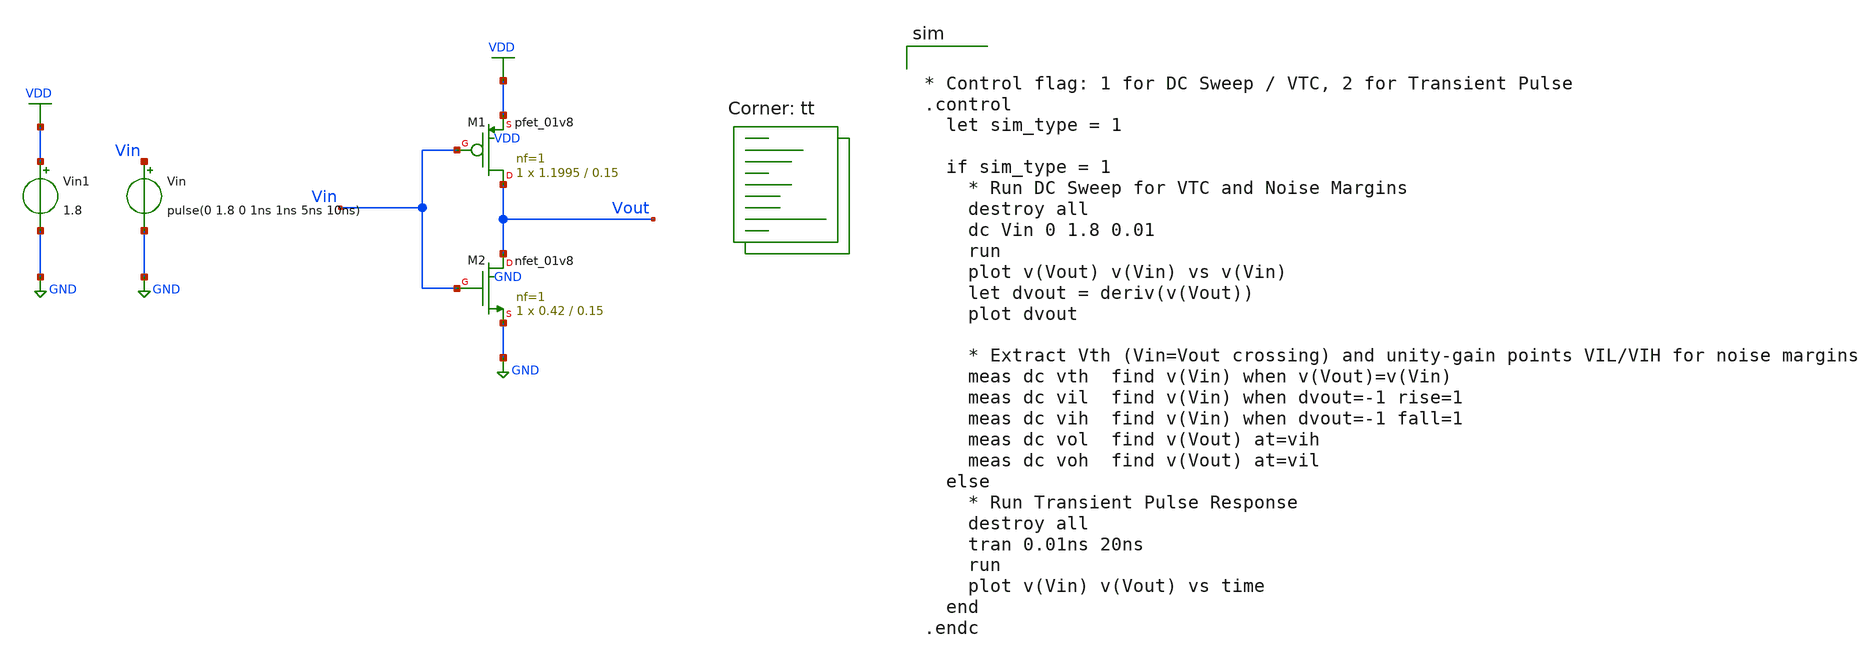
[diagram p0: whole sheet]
** sch_path: assignments/assignment2/assign1a.sch
**.subckt assign1a
Vin Vin GND pulse(0 1.8 0 1ns 1ns 5ns 10ns)
XM1 Vout Vin VDD VDD sky130_fd_pr__pfet_01v8 L=0.15 W=1.1995 nf=1 ad='int((nf+1)/2) * W/nf * 0.29' as='int((nf+2)/2) * W/nf * 0.29'
+ pd='2*int((nf+1)/2) * (W/nf + 0.29)' ps='2*int((nf+2)/2) * (W/nf + 0.29)' nrd='0.29 / W' nrs='0.29 / W'
+ sa=0 sb=0 sd=0 mult=1 m=1
XM2 Vout Vin GND GND sky130_fd_pr__nfet_01v8 L=0.15 W=0.42 nf=1 ad='int((nf+1)/2) * W/nf * 0.29' as='int((nf+2)/2) * W/nf * 0.29'
+ pd='2*int((nf+1)/2) * (W/nf + 0.29)' ps='2*int((nf+2)/2) * (W/nf + 0.29)' nrd='0.29 / W' nrs='0.29 / W'
+ sa=0 sb=0 sd=0 mult=1 m=1
Vin1 VDD GND 1.8
**** begin user architecture code


* Control flag: 1 for DC Sweep / VTC, 2 for Transient Pulse
.control
  let sim_type = 1

  if sim_type = 1
    * Run DC Sweep for VTC and Noise Margins
    destroy all
    dc Vin 0 1.8 0.01
    run
    plot v(Vout) v(Vin) vs v(Vin)
    let dvout = deriv(v(Vout))
    plot dvout

    * Extract Vth (Vin=Vout crossing) and unity-gain points VIL/VIH for noise margins
    meas dc vth  find v(Vin) when v(Vout)=v(Vin)
    meas dc vil  find v(Vin) when dvout=-1 rise=1
    meas dc vih  find v(Vin) when dvout=-1 fall=1
    meas dc vol  find v(Vout) at=vih
    meas dc voh  find v(Vout) at=vil
  else
    * Run Transient Pulse Response
    destroy all
    tran 0.01ns 20ns
    run
    plot v(Vin) v(Vout) vs time
  end
.endc


.lib $::SKYWATER_MODELS/sky130.lib.spice tt
**** end user architecture code
**.ends
.GLOBAL GND
.GLOBAL VDD
.end
